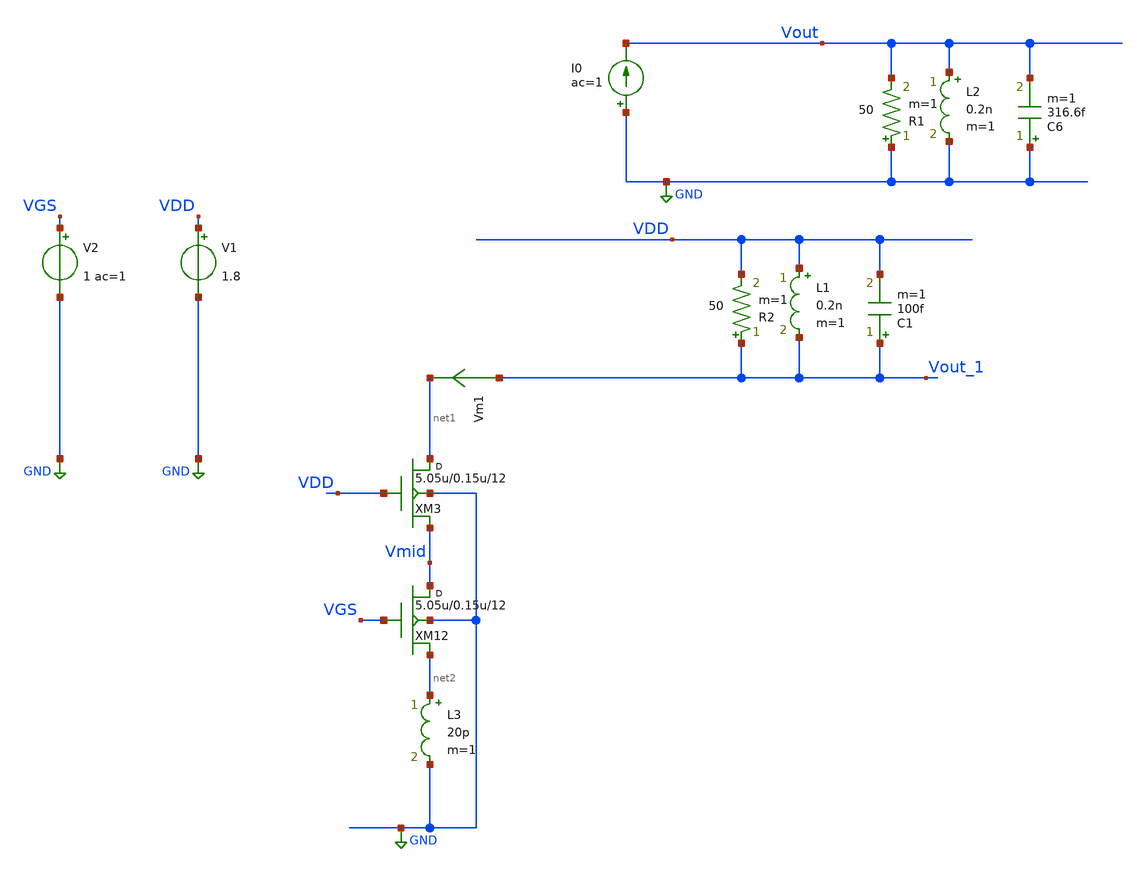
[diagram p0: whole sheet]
** sch_path: xschem/lna/Zout3.sch
**.subckt Zout3
I0 GND Vout ac=1
L2 Vout GND 0.2n m=1
C6 GND Vout 316.6f m=1
R1 GND Vout 50 m=1
XM12 Vmid VGS net2 GND sky130_fd_pr__rf_nfet_01v8_bM04W5p00L0p15_ext w=5.05u l=0.15u m=12
L1 VDD Vout_1 0.2n m=1
C1 Vout_1 VDD 100f m=1
R2 Vout_1 VDD 50 m=1
V1 VDD GND 1.8
V2 VGS GND 1 ac=1
XM3 net1 VDD Vmid GND sky130_fd_pr__rf_nfet_01v8_bM04W5p00L0p15_ext w=5.05u l=0.15u m=12
Vm1 Vout_1 net1 0
.save i(vm1)
L3 net2 GND 20p m=1
**** begin user architecture code


.subckt sky130_fd_pr__rf_nfet_01v8_bM04W5p00L0p15_ext DRAIN GATE SOURCE SUBSTRATE
X0 DRAIN GATE SOURCE SUBSTRATE sky130_fd_pr__nfet_01v8 ad=2.828e+12p pd=2.132e+07u as=4.242e+12p
+ ps=3.198e+07u w=5.05e+06u l=150000u
X1 SOURCE SUBSTRATE SUBSTRATE SUBSTRATE sky130_fd_pr__nfet_01v8 ad=0p pd=0u as=3.03e+12p
+ ps=2.14e+07u w=5.05e+06u l=150000u
X2 SOURCE GATE DRAIN SUBSTRATE sky130_fd_pr__nfet_01v8 ad=0p pd=0u as=0p ps=0u w=5.05e+06u l=150000u
X3 DRAIN GATE SOURCE SUBSTRATE sky130_fd_pr__nfet_01v8 ad=0p pd=0u as=0p ps=0u w=5.05e+06u l=150000u
X4 SUBSTRATE SUBSTRATE SOURCE SUBSTRATE sky130_fd_pr__nfet_01v8 ad=0p pd=0u as=0p ps=0u w=5.05e+06u
+ l=150000u
X5 SOURCE GATE DRAIN SUBSTRATE sky130_fd_pr__nfet_01v8 ad=0p pd=0u as=0p ps=0u w=5.05e+06u l=150000u
.ends
*.sp dec 1000 0.1e9 100e9 1
*.ac dec 1000 0.01e9 100e9
.option GMIN=1e-15
.control
save all
run
display

ac dec 10 100 100G
let phase = 180/PI*vp(Vout)

plot Vout_1 Vmid
*plot abs(real(Vout_1)) abs(real(Vmid))
plot abs(Vout_1) abs(real(Vmid))
plot imag(Vout_1)
plot vm1#branch

.endc



** opencircuitdesign pdks install
.lib $::SKYWATER_MODELS/sky130.lib.spice tt


**** end user architecture code
**.ends
.GLOBAL GND
.end
